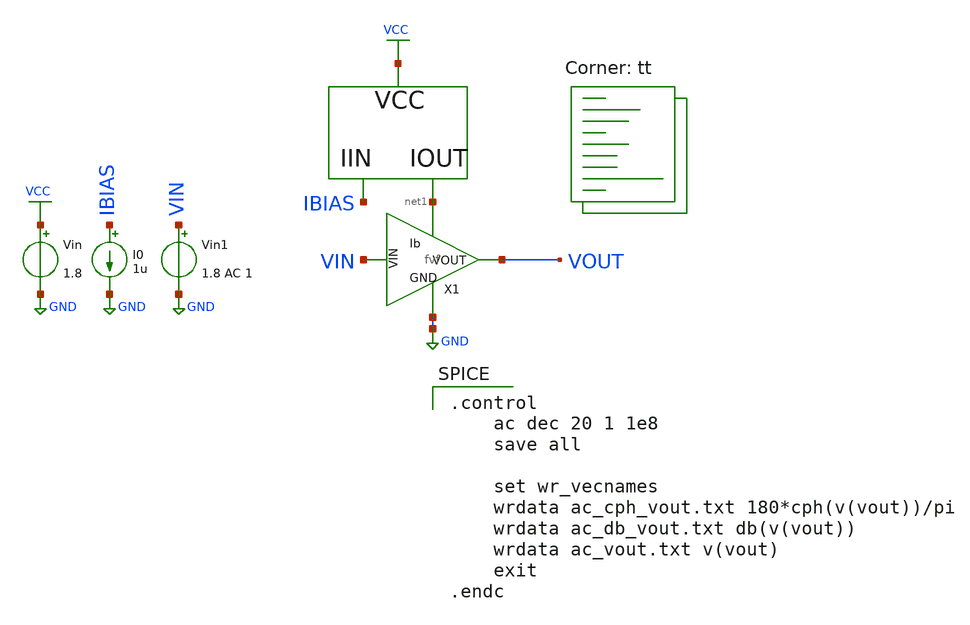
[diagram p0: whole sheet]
** sch_path: xschem/fvf_tb_ac.sch
**.subckt fvf_tb_ac
Vin VCC GND 1.8
I0 IBIAS GND 1u
X1 net1 GND VIN VOUT fvf
Vin1 VIN GND 1.8 AC 1
**** begin user architecture code
.lib $::SKYWATER_MODELS/sky130.lib.spice tt

.control
    ac dec 20 1 1e8
    save all

    set wr_vecnames
    wrdata ac_cph_vout.txt 180*cph(v(vout))/pi
    wrdata ac_db_vout.txt db(v(vout))
    wrdata ac_vout.txt v(vout)
    exit
.endc

**** end user architecture code
**.ends

* expanding   symbol:  /foss/designs/fvf-chipathon-2024/xschem/fvf.sym # of pins=4
** sym_path: xschem/fvf.sym
** sch_path: xschem/fvf.sch
.subckt fvf Ib GND VIN VOUT
*.ipin VIN
*.opin VOUT
*.iopin GND
*.ipin Ib
XM1 Ib VIN VOUT GND sky130_fd_pr__nfet_01v8 L=1 W=15 nf=1 ad='int((nf+1)/2) * W/nf * 0.29' as='int((nf+2)/2) * W/nf * 0.29'
+ pd='2*int((nf+1)/2) * (W/nf + 0.29)' ps='2*int((nf+2)/2) * (W/nf + 0.29)' nrd='0.29 / W' nrs='0.29 / W'
+ sa=0 sb=0 sd=0 mult=1 m=1
XM2 VOUT Ib GND GND sky130_fd_pr__nfet_01v8 L=1 W=15 nf=1 ad='int((nf+1)/2) * W/nf * 0.29' as='int((nf+2)/2) * W/nf * 0.29'
+ pd='2*int((nf+1)/2) * (W/nf + 0.29)' ps='2*int((nf+2)/2) * (W/nf + 0.29)' nrd='0.29 / W' nrs='0.29 / W'
+ sa=0 sb=0 sd=0 mult=1 m=1
.ends

.GLOBAL GND
.GLOBAL VCC
.end
